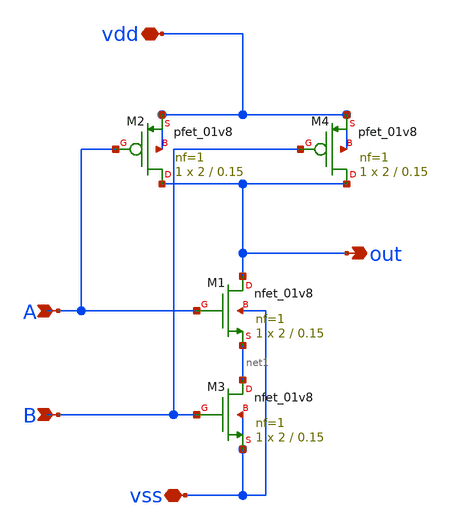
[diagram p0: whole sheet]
** sch_path: xschem/src/nand/nand.sch
**.subckt nand A B out vdd vss
*.ipin A
*.ipin B
*.opin out
*.iopin vdd
*.iopin vss
XM1 out A net1 vss sky130_fd_pr__nfet_01v8 L=0.15 W=2 nf=1 ad='int((nf+1)/2) * W/nf * 0.29' as='int((nf+2)/2) * W/nf * 0.29'
+ pd='2*int((nf+1)/2) * (W/nf + 0.29)' ps='2*int((nf+2)/2) * (W/nf + 0.29)' nrd='0.29 / W' nrs='0.29 / W'
+ sa=0 sb=0 sd=0 mult=1 m=1
XM2 out A vdd vdd sky130_fd_pr__pfet_01v8 L=0.15 W=2 nf=1 ad='int((nf+1)/2) * W/nf * 0.29' as='int((nf+2)/2) * W/nf * 0.29'
+ pd='2*int((nf+1)/2) * (W/nf + 0.29)' ps='2*int((nf+2)/2) * (W/nf + 0.29)' nrd='0.29 / W' nrs='0.29 / W'
+ sa=0 sb=0 sd=0 mult=1 m=1
XM3 net1 B vss vss sky130_fd_pr__nfet_01v8 L=0.15 W=2 nf=1 ad='int((nf+1)/2) * W/nf * 0.29' as='int((nf+2)/2) * W/nf * 0.29'
+ pd='2*int((nf+1)/2) * (W/nf + 0.29)' ps='2*int((nf+2)/2) * (W/nf + 0.29)' nrd='0.29 / W' nrs='0.29 / W'
+ sa=0 sb=0 sd=0 mult=1 m=1
XM4 out B vdd vdd sky130_fd_pr__pfet_01v8 L=0.15 W=2 nf=1 ad='int((nf+1)/2) * W/nf * 0.29' as='int((nf+2)/2) * W/nf * 0.29'
+ pd='2*int((nf+1)/2) * (W/nf + 0.29)' ps='2*int((nf+2)/2) * (W/nf + 0.29)' nrd='0.29 / W' nrs='0.29 / W'
+ sa=0 sb=0 sd=0 mult=1 m=1
**.ends
.end
